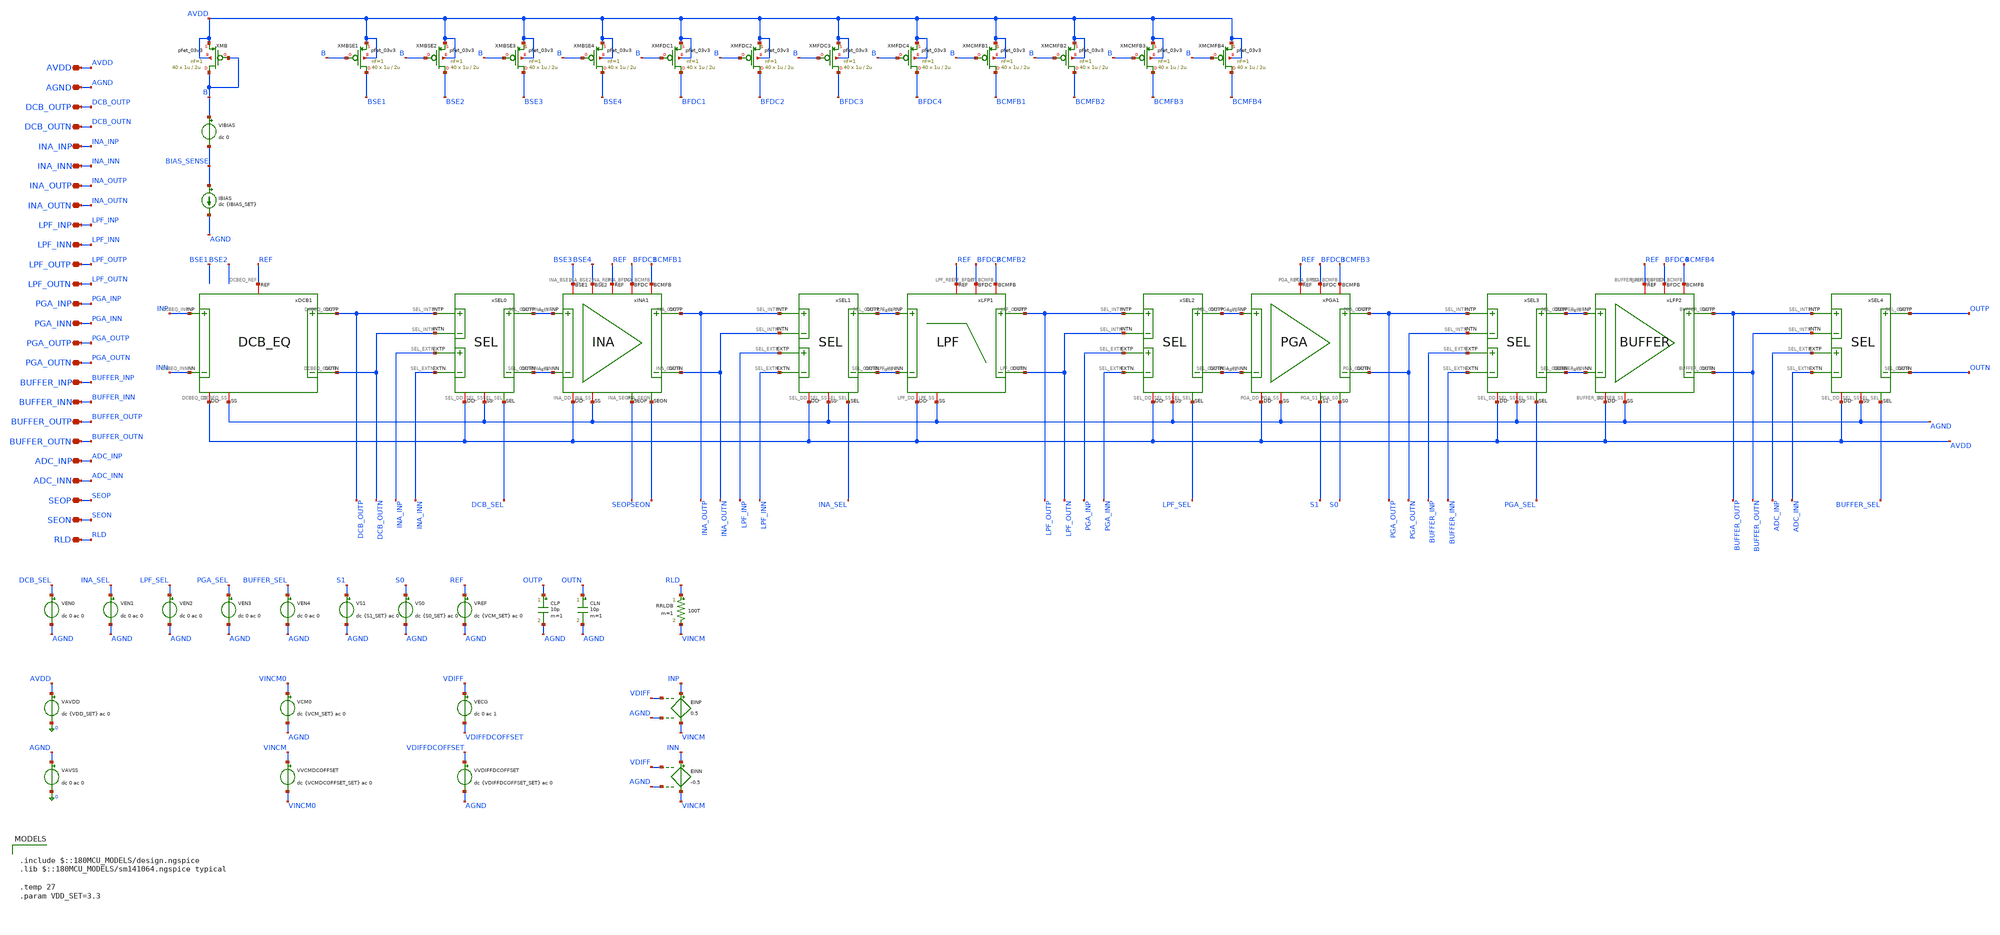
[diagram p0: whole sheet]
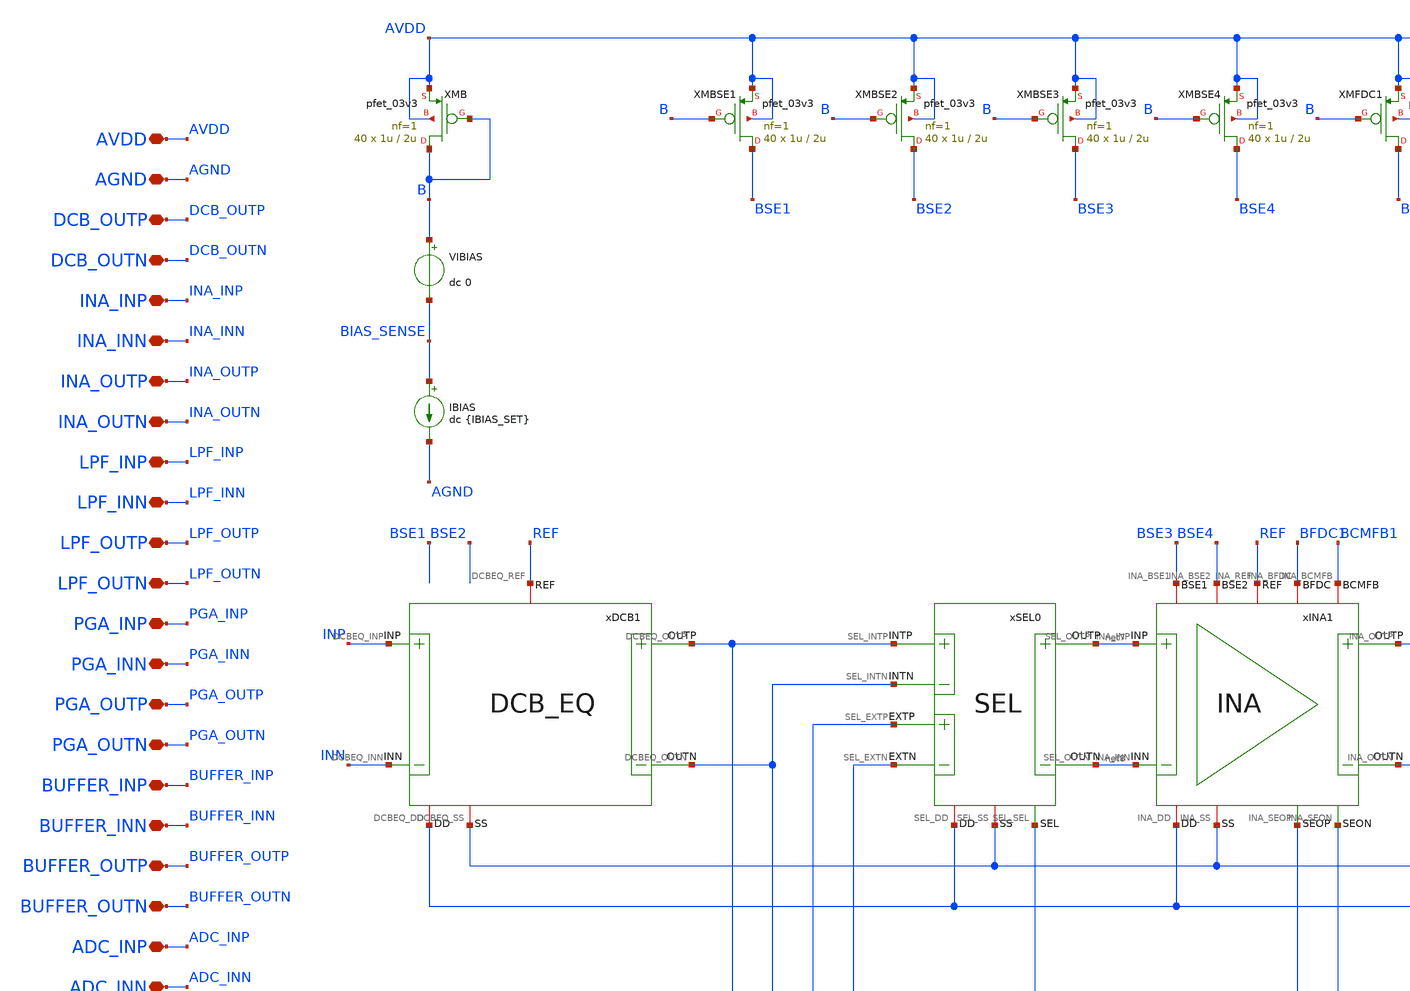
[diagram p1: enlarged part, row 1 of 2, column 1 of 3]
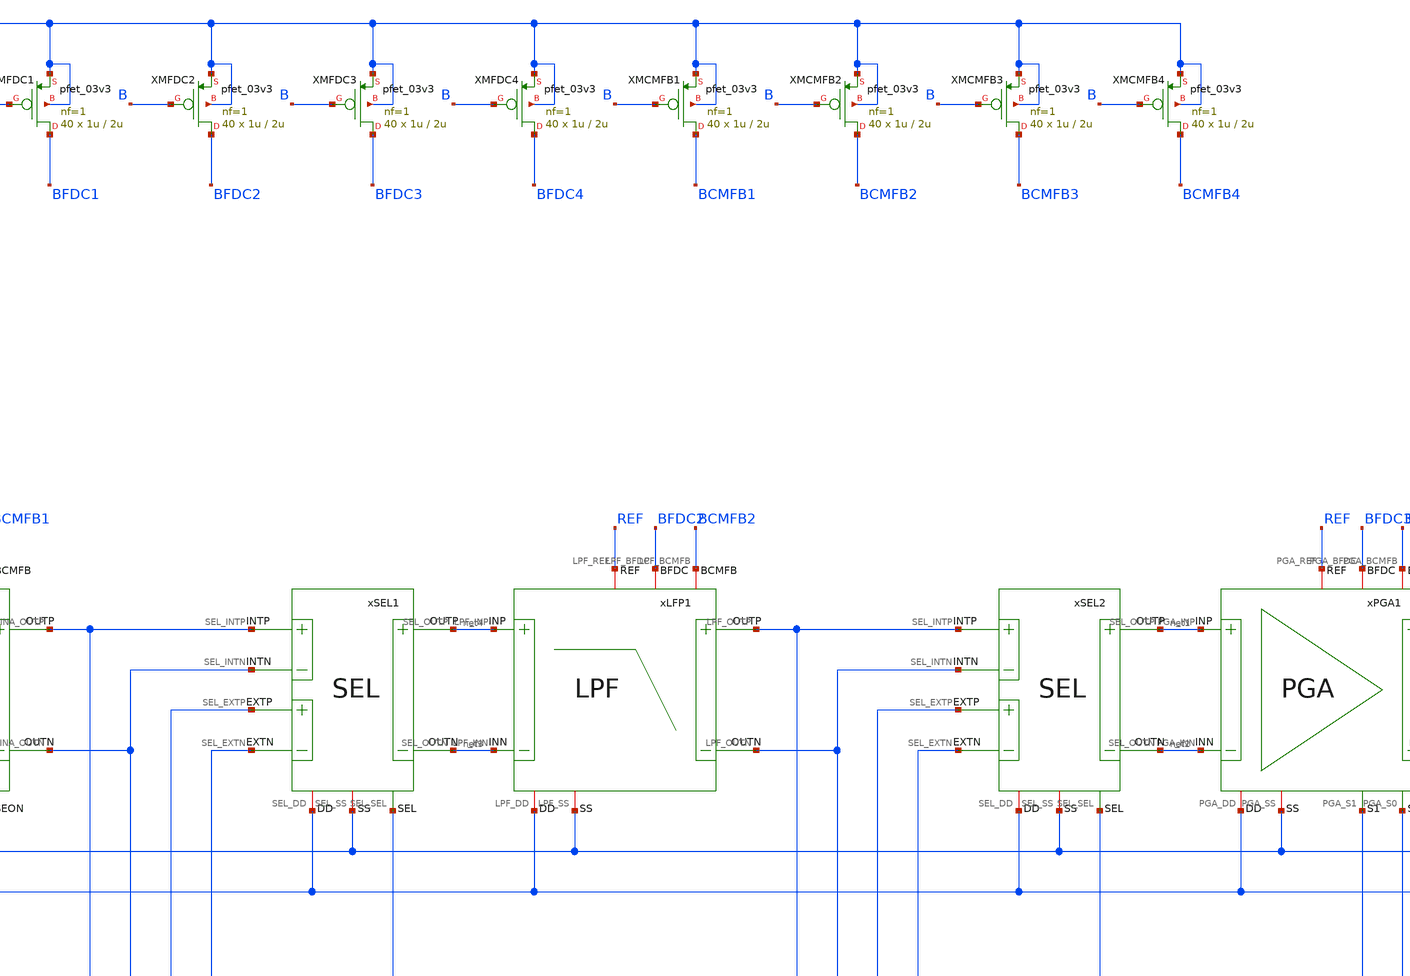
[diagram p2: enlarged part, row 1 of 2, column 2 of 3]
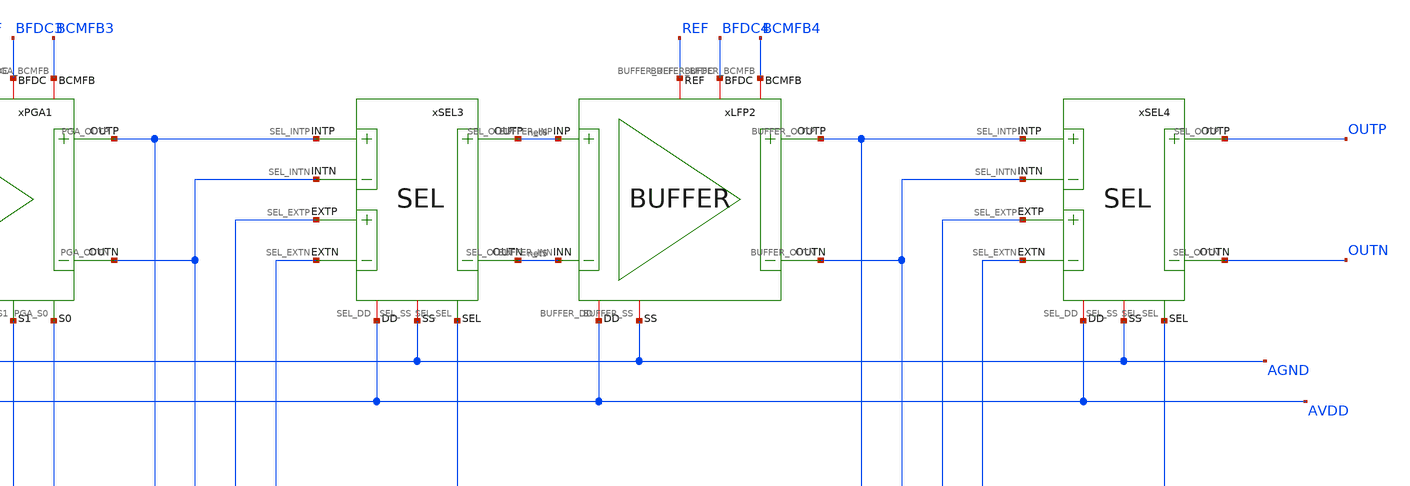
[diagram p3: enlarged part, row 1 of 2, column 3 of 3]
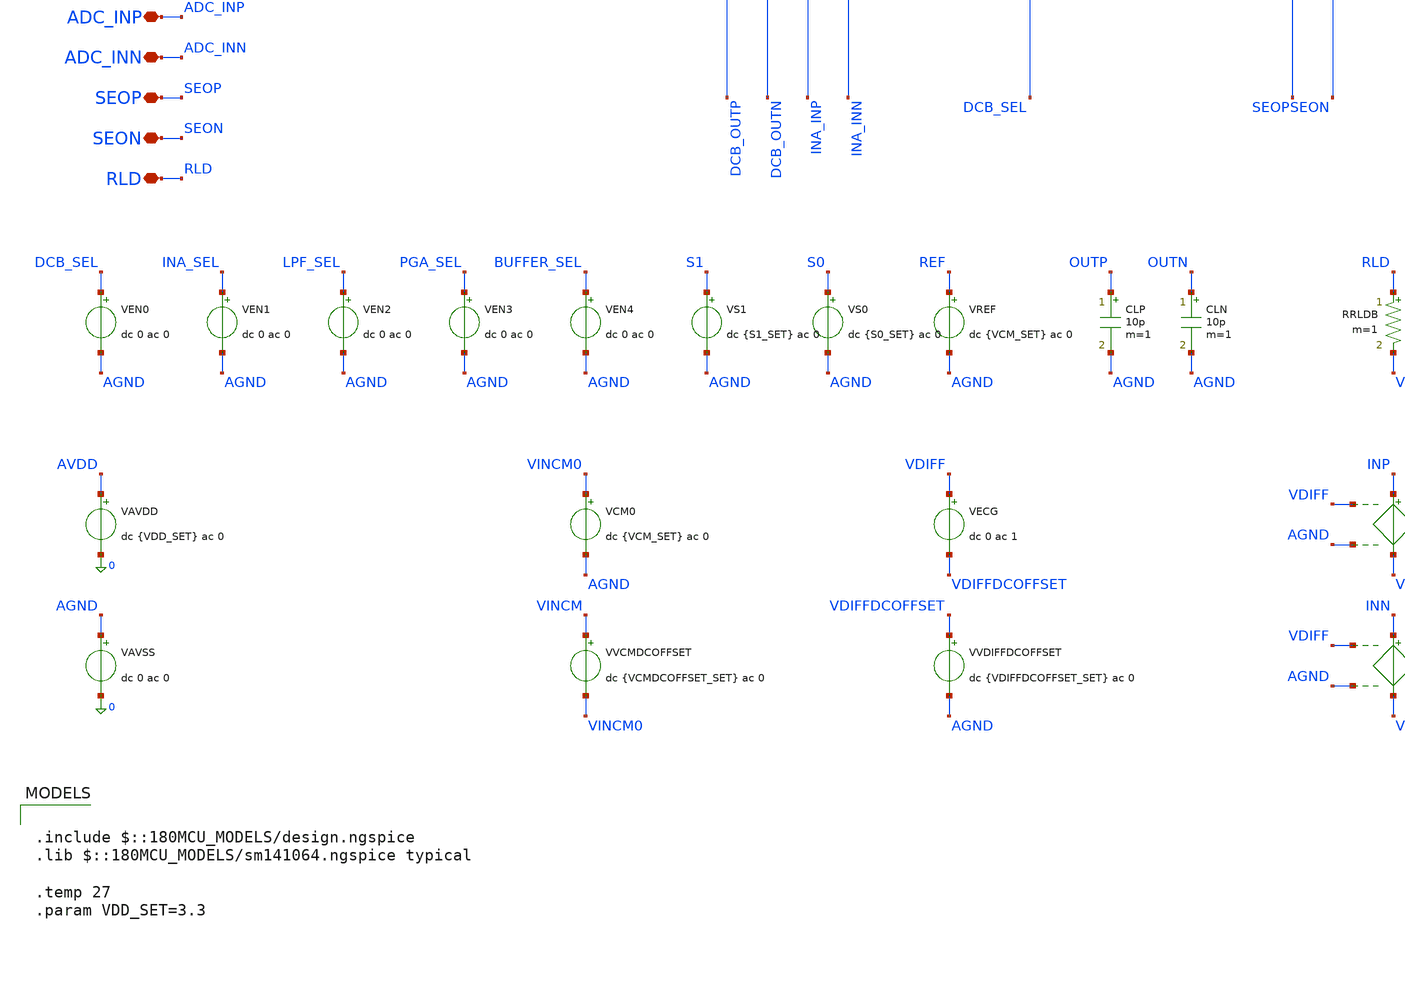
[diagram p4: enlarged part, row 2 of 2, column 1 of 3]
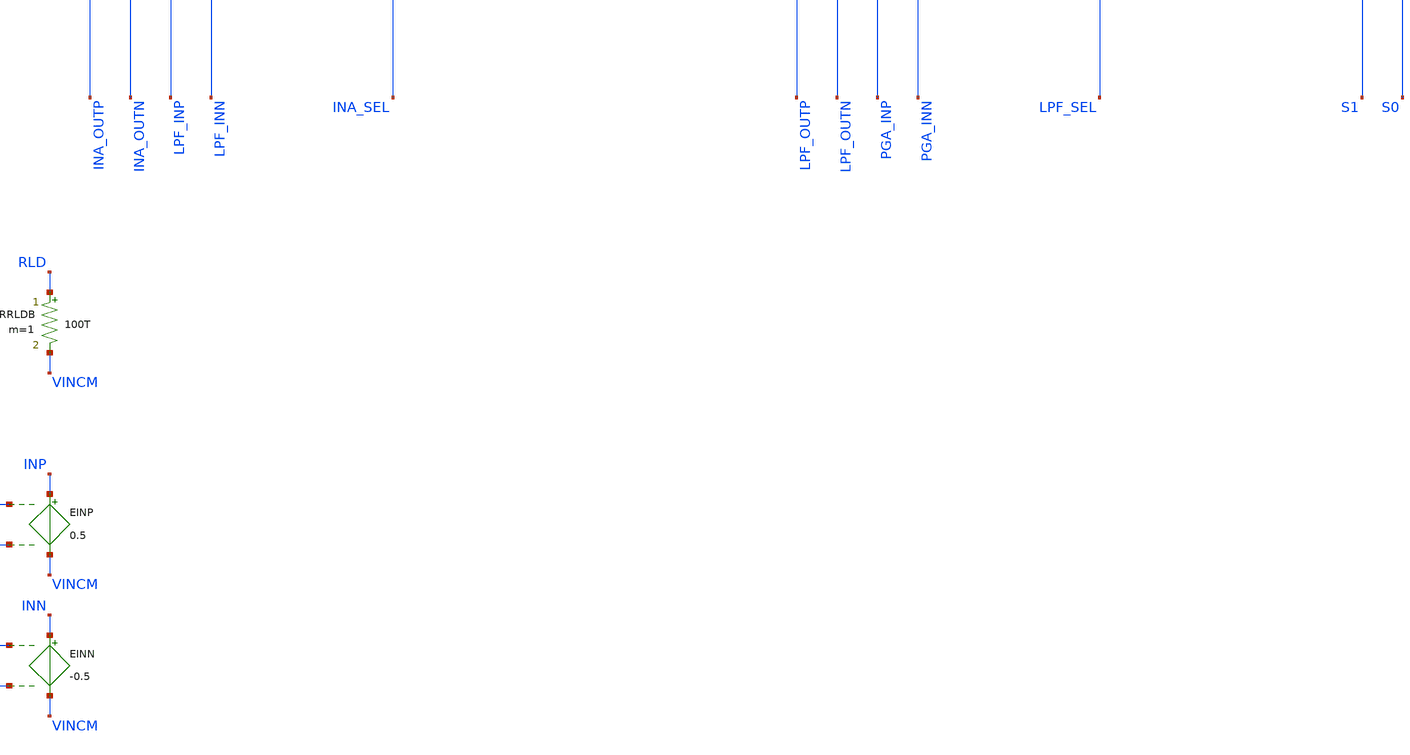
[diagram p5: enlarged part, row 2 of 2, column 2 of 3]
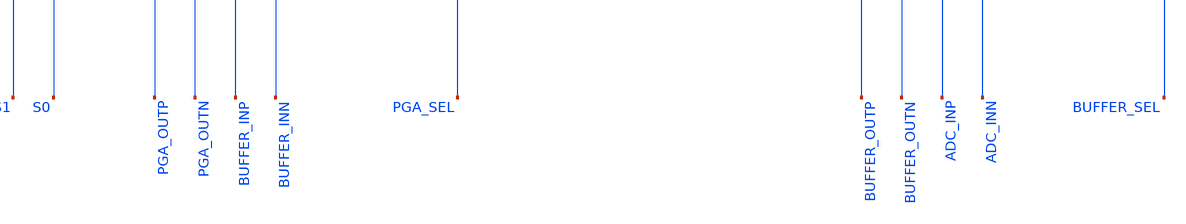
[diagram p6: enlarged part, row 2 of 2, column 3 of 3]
** sch_path: Design_Files/IC Design/Testbench/PATH/AC/PATH_TB_AC.sch
**.subckt PATH_TB_AC DCB_OUTP DCB_OUTN INA_INP INA_INN INA_OUTP INA_OUTN LPF_INP LPF_INN LPF_OUTP
*+ LPF_OUTN PGA_INP PGA_INN PGA_OUTP PGA_OUTN BUFFER_INP BUFFER_INN BUFFER_OUTP BUFFER_OUTN ADC_INP ADC_INN
*+ AVDD AGND SEOP SEON RLD
*.iopin DCB_OUTP
*.iopin DCB_OUTN
*.iopin INA_INP
*.iopin INA_INN
*.iopin INA_OUTP
*.iopin INA_OUTN
*.iopin LPF_INP
*.iopin LPF_INN
*.iopin LPF_OUTP
*.iopin LPF_OUTN
*.iopin PGA_INP
*.iopin PGA_INN
*.iopin PGA_OUTP
*.iopin PGA_OUTN
*.iopin BUFFER_INP
*.iopin BUFFER_INN
*.iopin BUFFER_OUTP
*.iopin BUFFER_OUTN
*.iopin ADC_INP
*.iopin ADC_INN
*.iopin AVDD
*.iopin AGND
*.iopin SEOP
*.iopin SEON
*.iopin RLD
CLP OUTP AGND 10p m=1
CLN OUTN AGND 10p m=1
VIBIAS B BIAS_SENSE dc 0
.save i(vibias)
IBIAS BIAS_SENSE AGND dc {IBIAS_SET}
VREF REF AGND dc {VCM_SET} ac 0
XMB B B AVDD AVDD pfet_03v3 L=2u W=1u nf=1 ad='int((nf+1)/2) * W/nf * 0.18u' as='int((nf+2)/2) * W/nf * 0.18u'
+ pd='2*int((nf+1)/2) * (W/nf + 0.18u)' ps='2*int((nf+2)/2) * (W/nf + 0.18u)' nrd='0.18u / W' nrs='0.18u / W'
+ sa=0 sb=0 sd=0 m=40
XMBSE3 BSE3 B AVDD AVDD pfet_03v3 L=2u W=1u nf=1 ad='int((nf+1)/2) * W/nf * 0.18u' as='int((nf+2)/2) * W/nf * 0.18u'
+ pd='2*int((nf+1)/2) * (W/nf + 0.18u)' ps='2*int((nf+2)/2) * (W/nf + 0.18u)' nrd='0.18u / W' nrs='0.18u / W'
+ sa=0 sb=0 sd=0 m=40
XMBSE4 BSE4 B AVDD AVDD pfet_03v3 L=2u W=1u nf=1 ad='int((nf+1)/2) * W/nf * 0.18u' as='int((nf+2)/2) * W/nf * 0.18u'
+ pd='2*int((nf+1)/2) * (W/nf + 0.18u)' ps='2*int((nf+2)/2) * (W/nf + 0.18u)' nrd='0.18u / W' nrs='0.18u / W'
+ sa=0 sb=0 sd=0 m=40
XMFDC1 BFDC1 B AVDD AVDD pfet_03v3 L=2u W=1u nf=1 ad='int((nf+1)/2) * W/nf * 0.18u' as='int((nf+2)/2) * W/nf * 0.18u'
+ pd='2*int((nf+1)/2) * (W/nf + 0.18u)' ps='2*int((nf+2)/2) * (W/nf + 0.18u)' nrd='0.18u / W' nrs='0.18u / W'
+ sa=0 sb=0 sd=0 m=40
XMFDC2 BFDC2 B AVDD AVDD pfet_03v3 L=2u W=1u nf=1 ad='int((nf+1)/2) * W/nf * 0.18u' as='int((nf+2)/2) * W/nf * 0.18u'
+ pd='2*int((nf+1)/2) * (W/nf + 0.18u)' ps='2*int((nf+2)/2) * (W/nf + 0.18u)' nrd='0.18u / W' nrs='0.18u / W'
+ sa=0 sb=0 sd=0 m=40
XMFDC3 BFDC3 B AVDD AVDD pfet_03v3 L=2u W=1u nf=1 ad='int((nf+1)/2) * W/nf * 0.18u' as='int((nf+2)/2) * W/nf * 0.18u'
+ pd='2*int((nf+1)/2) * (W/nf + 0.18u)' ps='2*int((nf+2)/2) * (W/nf + 0.18u)' nrd='0.18u / W' nrs='0.18u / W'
+ sa=0 sb=0 sd=0 m=40
XMFDC4 BFDC4 B AVDD AVDD pfet_03v3 L=2u W=1u nf=1 ad='int((nf+1)/2) * W/nf * 0.18u' as='int((nf+2)/2) * W/nf * 0.18u'
+ pd='2*int((nf+1)/2) * (W/nf + 0.18u)' ps='2*int((nf+2)/2) * (W/nf + 0.18u)' nrd='0.18u / W' nrs='0.18u / W'
+ sa=0 sb=0 sd=0 m=40
XMCMFB1 BCMFB1 B AVDD AVDD pfet_03v3 L=2u W=1u nf=1 ad='int((nf+1)/2) * W/nf * 0.18u' as='int((nf+2)/2) * W/nf * 0.18u'
+ pd='2*int((nf+1)/2) * (W/nf + 0.18u)' ps='2*int((nf+2)/2) * (W/nf + 0.18u)' nrd='0.18u / W' nrs='0.18u / W'
+ sa=0 sb=0 sd=0 m=40
XMCMFB2 BCMFB2 B AVDD AVDD pfet_03v3 L=2u W=1u nf=1 ad='int((nf+1)/2) * W/nf * 0.18u' as='int((nf+2)/2) * W/nf * 0.18u'
+ pd='2*int((nf+1)/2) * (W/nf + 0.18u)' ps='2*int((nf+2)/2) * (W/nf + 0.18u)' nrd='0.18u / W' nrs='0.18u / W'
+ sa=0 sb=0 sd=0 m=40
xLFP1 AVDD AGND net4 net3 LPF_OUTN BFDC2 LPF_OUTP BCMFB2 REF LPF
xPGA1 AVDD AGND net1 net2 PGA_OUTN BFDC3 PGA_OUTP BCMFB3 REF S1 S0 PGA
xSEL1 AVDD AGND INA_OUTP INA_OUTN net3 net4 LPF_INP LPF_INN INA_SEL SEL
xINA1 AVDD AGND net7 net8 INA_OUTN BFDC1 INA_OUTP BCMFB1 REF SEON SEOP BSE3 BSE4 INA
xSEL2 AVDD AGND LPF_OUTP LPF_OUTN net2 net1 PGA_INP PGA_INN LPF_SEL SEL
xSEL3 AVDD AGND PGA_OUTP PGA_OUTN net5 net6 BUFFER_INP BUFFER_INN PGA_SEL SEL
xSEL4 AVDD AGND BUFFER_OUTP BUFFER_OUTN OUTN OUTP ADC_INP ADC_INN BUFFER_SEL SEL
xLFP2 AVDD AGND net6 net5 BUFFER_OUTN BFDC4 BUFFER_OUTP BCMFB4 REF BUFFER
XMCMFB3 BCMFB3 B AVDD AVDD pfet_03v3 L=2u W=1u nf=1 ad='int((nf+1)/2) * W/nf * 0.18u' as='int((nf+2)/2) * W/nf * 0.18u'
+ pd='2*int((nf+1)/2) * (W/nf + 0.18u)' ps='2*int((nf+2)/2) * (W/nf + 0.18u)' nrd='0.18u / W' nrs='0.18u / W'
+ sa=0 sb=0 sd=0 m=40
XMCMFB4 BCMFB4 B AVDD AVDD pfet_03v3 L=2u W=1u nf=1 ad='int((nf+1)/2) * W/nf * 0.18u' as='int((nf+2)/2) * W/nf * 0.18u'
+ pd='2*int((nf+1)/2) * (W/nf + 0.18u)' ps='2*int((nf+2)/2) * (W/nf + 0.18u)' nrd='0.18u / W' nrs='0.18u / W'
+ sa=0 sb=0 sd=0 m=40
VEN1 INA_SEL AGND dc 0 ac 0
.save i(ven1)
VS0 S0 AGND dc {S0_SET} ac 0
VS1 S1 AGND dc {S1_SET} ac 0
xSEL0 AVDD AGND DCB_OUTP DCB_OUTN net8 net7 INA_INP INA_INN DCB_SEL SEL
VEN2 LPF_SEL AGND dc 0 ac 0
.save i(ven2)
VEN3 PGA_SEL AGND dc 0 ac 0
.save i(ven3)
VEN4 BUFFER_SEL AGND dc 0 ac 0
.save i(ven4)
VEN0 DCB_SEL AGND dc 0 ac 0
.save i(ven0)
xDCB1 AVDD AGND INP INN DCB_OUTP DCB_OUTN REF DCB_EQ
VAVDD AVDD 0 dc {VDD_SET} ac 0
.save i(vavdd)
VAVSS AGND 0 dc 0 ac 0
.save i(vavss)
VCM0 VINCM0 AGND dc {VCM_SET} ac 0
VVCMDCOFFSET VINCM VINCM0 dc {VCMDCOFFSET_SET} ac 0
VECG VDIFF VDIFFDCOFFSET dc 0 ac 1
VVDIFFDCOFFSET VDIFFDCOFFSET AGND dc {VDIFFDCOFFSET_SET} ac 0
EINP INP VINCM VDIFF AGND 0.5
EINN INN VINCM VDIFF AGND -0.5
RRLDB RLD VINCM 100T m=1
XMBSE1 BSE1 B AVDD AVDD pfet_03v3 L=2u W=1u nf=1 ad='int((nf+1)/2) * W/nf * 0.18u' as='int((nf+2)/2) * W/nf * 0.18u'
+ pd='2*int((nf+1)/2) * (W/nf + 0.18u)' ps='2*int((nf+2)/2) * (W/nf + 0.18u)' nrd='0.18u / W' nrs='0.18u / W'
+ sa=0 sb=0 sd=0 m=40
XMBSE2 BSE2 B AVDD AVDD pfet_03v3 L=2u W=1u nf=1 ad='int((nf+1)/2) * W/nf * 0.18u' as='int((nf+2)/2) * W/nf * 0.18u'
+ pd='2*int((nf+1)/2) * (W/nf + 0.18u)' ps='2*int((nf+2)/2) * (W/nf + 0.18u)' nrd='0.18u / W' nrs='0.18u / W'
+ sa=0 sb=0 sd=0 m=40
**** begin user architecture code

.include $::180MCU_MODELS/design.ngspice
.lib $::180MCU_MODELS/sm141064.ngspice typical

.temp 27
.param VDD_SET=3.3



.param VCM_SET={VDD_SET/2}

.param VCMDCOFFSET_SET=0
.param VDIFFDCOFFSET_SET=0

.param IBIAS_SET=40u

.param S1_SET=3.3
.param S0_SET=3.3

.options method=gear
.options sparse

.options gmin=1e-12
.options rshunt=100T

.options reltol=1e-3
.options abstol=1e-12
.options vntol=1u
.options chgtol=1e-14

.options itl1=2000
.options itl2=1000
.options itl4=2000

.nodeset v(B)=2.3

.nodeset v(INP)={VCM_SET}
.nodeset v(INN)={VCM_SET}

.nodeset v(DCB_OUTP)={VCM_SET}
.nodeset v(DCB_OUTN)={VCM_SET}

.nodeset v(INA_OUTP)={VCM_SET}
.nodeset v(INA_OUTN)={VCM_SET}

.nodeset v(LPF_OUTP)={VCM_SET}
.nodeset v(LPF_OUTN)={VCM_SET}

.nodeset v(PGA_OUTP)={VCM_SET}
.nodeset v(PGA_OUTN)={VCM_SET}

.nodeset v(BUFFER_OUTP)={VCM_SET}
.nodeset v(BUFFER_OUTN)={VCM_SET}

.nodeset v(OUTP)={VCM_SET}
.nodeset v(OUTN)={VCM_SET}

.nodeset v(RLD)={VCM_SET}

.save all





.control

destroy all

set noaskquit
set wr_singlescale
unset wr_vecnames
set appendwrite
set units=degrees

option numdgt=15
option sparse

shell mkdir -p
+ /foss/designs/ECG_Acquisition_IC/Measurement_Results/IC_Simulation/PATH/NOM.Result_txt

shell rm -f
+ /foss/designs/ECG_Acquisition_IC/Measurement_Results/IC_Simulation/PATH/NOM.Result_txt/NOM.op.txt
shell rm -f
+ /foss/designs/ECG_Acquisition_IC/Measurement_Results/IC_Simulation/PATH/NOM.Result_txt/NOM.diff_ac.txt
shell rm -f
+ /foss/designs/ECG_Acquisition_IC/Measurement_Results/IC_Simulation/PATH/NOM.Result_txt/NOM.cmrr_ac.txt
shell rm -f
+ /foss/designs/ECG_Acquisition_IC/Measurement_Results/IC_Simulation/PATH/NOM.Result_txt/NOM.psrrp_ac.txt
shell rm -f
+ /foss/designs/ECG_Acquisition_IC/Measurement_Results/IC_Simulation/PATH/NOM.Result_txt/NOM.psrrn_ac.txt


* OP: G2 and G16
foreach gaincfg 0 1

    if $gaincfg = 0
        alterparam S1_SET=0
        alterparam S0_SET=0
    else
        alterparam S1_SET=3.3
        alterparam S0_SET=3.3
    end

    reset
    save all

    alter @VECG[ACMAG]=0
    alter @VECG[ACPHASE]=0

    alter @VCM0[ACMAG]=0
    alter @VCM0[ACPHASE]=0

    alter @VAVDD[ACMAG]=0
    alter @VAVDD[ACPHASE]=0

    alter @VAVSS[ACMAG]=0
    alter @VAVSS[ACPHASE]=0

    op

    let op_index=0

    if $gaincfg = 0
        let op_pga_gain=op_index*0+2
    else
        let op_pga_gain=op_index*0+16
    end

    let op_vdd=v(AVDD)-v(AGND)

    let op_vinp=v(INP)-v(AGND)
    let op_vinn=v(INN)-v(AGND)

    let op_vin_cm=0.5*(v(INP)+v(INN))-v(AGND)
    let op_vin_diff=v(INP)-v(INN)

    let op_outp=v(OUTP)-v(AGND)
    let op_outn=v(OUTN)-v(AGND)

    let op_vout_cm=0.5*(v(OUTP)+v(OUTN))-v(AGND)
    let op_vout_diff=v(OUTP)-v(OUTN)

    let op_rld=v(RLD)-v(AGND)
    let op_ref=v(REF)-v(AGND)

    let op_ibias=abs(vibias#branch)
    let op_idd=abs(vavdd#branch)
    let op_power=op_vdd*op_idd

    setscale op_index

    wrdata
+ /foss/designs/ECG_Acquisition_IC/Measurement_Results/IC_Simulation/PATH/NOM.Result_txt/NOM.op.txt op_pga_gain op_vdd op_vinp op_vinn op_vin_cm op_vin_diff op_outp op_outn op_vout_cm op_vout_diff
+ op_rld op_ref op_ibias op_idd op_power

    destroy $curplot

end


* Differential AC: G2 and G16
foreach gaincfg 0 1

    if $gaincfg = 0
        alterparam S1_SET=0
        alterparam S0_SET=0
    else
        alterparam S1_SET=3.3
        alterparam S0_SET=3.3
    end

    reset
    save all

    alter @VECG[ACMAG]=1
    alter @VECG[ACPHASE]=0

    alter @VCM0[ACMAG]=0
    alter @VCM0[ACPHASE]=0

    alter @VAVDD[ACMAG]=0
    alter @VAVDD[ACPHASE]=0

    alter @VAVSS[ACMAG]=0
    alter @VAVSS[ACPHASE]=0

    ac dec 200 0.001 10k

    if $gaincfg = 0
        let ac_pga_gain=frequency*0+2
    else
        let ac_pga_gain=frequency*0+16
    end

    let ac_vin_diff=v(INP)-v(INN)
    let ac_vout_diff=v(OUTP)-v(OUTN)
    let ac_vout_cm=0.5*(v(OUTP)+v(OUTN))-v(AGND)

    let ac_hdiff=ac_vout_diff/ac_vin_diff

    let vin_diff_real=real(ac_vin_diff)
    let vin_diff_imag=imag(ac_vin_diff)
    let vin_diff_mag=mag(ac_vin_diff)
    let vin_diff_phase=ph(ac_vin_diff)

    let vout_diff_real=real(ac_vout_diff)
    let vout_diff_imag=imag(ac_vout_diff)
    let vout_diff_mag=mag(ac_vout_diff)
    let vout_diff_phase=ph(ac_vout_diff)

    let vout_cm_real=real(ac_vout_cm)
    let vout_cm_imag=imag(ac_vout_cm)

    let hdiff_real=real(ac_hdiff)
    let hdiff_imag=imag(ac_hdiff)
    let hdiff_mag=mag(ac_hdiff)
    let hdiff_db=db(ac_hdiff)
    let hdiff_phase=ph(ac_hdiff)

    setscale frequency

    wrdata
+ /foss/designs/ECG_Acquisition_IC/Measurement_Results/IC_Simulation/PATH/NOM.Result_txt/NOM.diff_ac.txt ac_pga_gain vin_diff_real vin_diff_imag vin_diff_mag vin_diff_phase vout_diff_real vout_diff_imag
+ vout_diff_mag vout_diff_phase vout_cm_real vout_cm_imag hdiff_real hdiff_imag hdiff_mag hdiff_db hdiff_phase

    destroy $curplot

end


* CMRR AC: G2 and G16
foreach gaincfg 0 1

    if $gaincfg = 0
        alterparam S1_SET=0
        alterparam S0_SET=0
    else
        alterparam S1_SET=3.3
        alterparam S0_SET=3.3
    end

    reset
    save all

    alter @VECG[ACMAG]=0
    alter @VECG[ACPHASE]=0

    alter @VCM0[ACMAG]=1
    alter @VCM0[ACPHASE]=0

    alter @VAVDD[ACMAG]=0
    alter @VAVDD[ACPHASE]=0

    alter @VAVSS[ACMAG]=0
    alter @VAVSS[ACPHASE]=0

    ac dec 200 0.001 10k

    if $gaincfg = 0
        let ac_pga_gain=frequency*0+2
    else
        let ac_pga_gain=frequency*0+16
    end

    let ac_vin_cm=0.5*(v(INP)+v(INN))-v(AGND)
    let ac_vout_diff=v(OUTP)-v(OUTN)
    let ac_vout_cm=0.5*(v(OUTP)+v(OUTN))-v(AGND)

    let ac_hcm_diff=ac_vout_diff/ac_vin_cm

    let vin_cm_real=real(ac_vin_cm)
    let vin_cm_imag=imag(ac_vin_cm)
    let vin_cm_mag=mag(ac_vin_cm)
    let vin_cm_phase=ph(ac_vin_cm)

    let vout_diff_real=real(ac_vout_diff)
    let vout_diff_imag=imag(ac_vout_diff)

    let vout_cm_real=real(ac_vout_cm)
    let vout_cm_imag=imag(ac_vout_cm)

    let hcm_diff_real=real(ac_hcm_diff)
    let hcm_diff_imag=imag(ac_hcm_diff)
    let hcm_diff_mag=mag(ac_hcm_diff)
    let hcm_diff_db=db(ac_hcm_diff)
    let hcm_diff_phase=ph(ac_hcm_diff)

    setscale frequency

    wrdata
+ /foss/designs/ECG_Acquisition_IC/Measurement_Results/IC_Simulation/PATH/NOM.Result_txt/NOM.cmrr_ac.txt ac_pga_gain vin_cm_real vin_cm_imag vin_cm_mag vin_cm_phase vout_diff_real vout_diff_imag
+ vout_cm_real vout_cm_imag hcm_diff_real hcm_diff_imag hcm_diff_mag hcm_diff_db hcm_diff_phase

    destroy $curplot

end


* PSRR+ AC: G2 and G16
foreach gaincfg 0 1

    if $gaincfg = 0
        alterparam S1_SET=0
        alterparam S0_SET=0
    else
        alterparam S1_SET=3.3
        alterparam S0_SET=3.3
    end

    reset
    save all

    alter @VECG[ACMAG]=0
    alter @VECG[ACPHASE]=0

    alter @VCM0[ACMAG]=0
    alter @VCM0[ACPHASE]=0

    alter @VAVDD[ACMAG]=1
    alter @VAVDD[ACPHASE]=0

    alter @VAVSS[ACMAG]=0
    alter @VAVSS[ACPHASE]=0

    ac dec 200 0.001 10k

    if $gaincfg = 0
        let ac_pga_gain=frequency*0+2
    else
        let ac_pga_gain=frequency*0+16
    end

    let ac_supply=v(AVDD)-v(AGND)
    let ac_vout_diff=v(OUTP)-v(OUTN)
    let ac_vout_cm=0.5*(v(OUTP)+v(OUTN))-v(AGND)

    let ac_hpsrrp=ac_vout_diff/ac_supply

    let supply_real=real(ac_supply)
    let supply_imag=imag(ac_supply)
    let supply_mag=mag(ac_supply)
    let supply_phase=ph(ac_supply)

    let vout_diff_real=real(ac_vout_diff)
    let vout_diff_imag=imag(ac_vout_diff)

    let vout_cm_real=real(ac_vout_cm)
    let vout_cm_imag=imag(ac_vout_cm)

    let hpsrrp_real=real(ac_hpsrrp)
    let hpsrrp_imag=imag(ac_hpsrrp)
    let hpsrrp_mag=mag(ac_hpsrrp)
    let hpsrrp_db=db(ac_hpsrrp)
    let hpsrrp_phase=ph(ac_hpsrrp)

    setscale frequency

    wrdata
+ /foss/designs/ECG_Acquisition_IC/Measurement_Results/IC_Simulation/PATH/NOM.Result_txt/NOM.psrrp_ac.txt ac_pga_gain supply_real supply_imag supply_mag supply_phase vout_diff_real vout_diff_imag
+ vout_cm_real vout_cm_imag hpsrrp_real hpsrrp_imag hpsrrp_mag hpsrrp_db hpsrrp_phase

    destroy $curplot

end


* PSRR- AC: G2 and G16
foreach gaincfg 0 1

    if $gaincfg = 0
        alterparam S1_SET=0
        alterparam S0_SET=0
    else
        alterparam S1_SET=3.3
        alterparam S0_SET=3.3
    end

    reset
    save all

    alter @VECG[ACMAG]=0
    alter @VECG[ACPHASE]=0

    alter @VCM0[ACMAG]=0
    alter @VCM0[ACPHASE]=0

    alter @VAVDD[ACMAG]=0
    alter @VAVDD[ACPHASE]=0

    alter @VAVSS[ACMAG]=1
    alter @VAVSS[ACPHASE]=0

    ac dec 200 0.001 10k

    if $gaincfg = 0
        let ac_pga_gain=frequency*0+2
    else
        let ac_pga_gain=frequency*0+16
    end

    let ac_supply=v(AGND)
    let ac_vout_diff=v(OUTP)-v(OUTN)
    let ac_vout_cm=0.5*(v(OUTP)+v(OUTN))-v(AGND)

    let ac_hpsrrn=ac_vout_diff/ac_supply

    let supply_real=real(ac_supply)
    let supply_imag=imag(ac_supply)
    let supply_mag=mag(ac_supply)
    let supply_phase=ph(ac_supply)

    let vout_diff_real=real(ac_vout_diff)
    let vout_diff_imag=imag(ac_vout_diff)

    let vout_cm_real=real(ac_vout_cm)
    let vout_cm_imag=imag(ac_vout_cm)

    let hpsrrn_real=real(ac_hpsrrn)
    let hpsrrn_imag=imag(ac_hpsrrn)
    let hpsrrn_mag=mag(ac_hpsrrn)
    let hpsrrn_db=db(ac_hpsrrn)
    let hpsrrn_phase=ph(ac_hpsrrn)

    setscale frequency

    wrdata
+ /foss/designs/ECG_Acquisition_IC/Measurement_Results/IC_Simulation/PATH/NOM.Result_txt/NOM.psrrn_ac.txt ac_pga_gain supply_real supply_imag supply_mag supply_phase vout_diff_real vout_diff_imag
+ vout_cm_real vout_cm_imag hpsrrn_real hpsrrn_imag hpsrrn_mag hpsrrn_db hpsrrn_phase

    destroy $curplot

end


* Last simulated gain is already G16

quit
.endc


**** end user architecture code
**.ends

* expanding   symbol:  ECG_Acquisition_IC/Design_Files/IC Design/Schematic/LPF/LPF.sym # of pins=9
** sym_path: Design_Files/IC Design/Schematic/LPF/LPF.sym
** sch_path: Design_Files/IC Design/Schematic/LPF/LPF.sch
.subckt LPF LPF_DD LPF_SS LPF_INP LPF_INN LPF_OUTN LPF_BFDC LPF_OUTP LPF_BCMFB LPF_REF
*.iopin LPF_DD
*.iopin LPF_SS
*.ipin LPF_INP
*.ipin LPF_INN
*.opin LPF_OUTP
*.iopin LPF_BFDC
*.opin LPF_OUTN
*.iopin LPF_BCMFB
*.iopin LPF_REF
RFBP net1 LPF_OUTN 3.7Meg m=1
xFDOTA1 LPF_DD LPF_SS net1 net2 LPF_OUTN LPF_BFDC LPF_OUTP LPF_BCMFB LPF_REF LPF_VOCM FD_OTA
RINN LPF_INN net2 3.7Meg m=1
RINP LPF_INP net1 3.7Meg m=1
RFBN net2 LPF_OUTP 3.7Meg m=1
CLPFP net1 LPF_OUTN 20p m=5
CLPFN net2 LPF_OUTP 20p m=5
.ends


* expanding   symbol:  ECG_Acquisition_IC/Design_Files/IC Design/Schematic/PGA/PGA.sym # of pins=11
** sym_path: Design_Files/IC Design/Schematic/PGA/PGA.sym
** sch_path: Design_Files/IC Design/Schematic/PGA/PGA.sch
.subckt PGA PGA_DD PGA_SS PGA_INP PGA_INN PGA_OUTN PGA_BFDC PGA_OUTP PGA_BCMFB PGA_REF PGA_S1 PGA_S0
*.iopin PGA_DD
*.iopin PGA_SS
*.ipin PGA_INP
*.ipin PGA_INN
*.opin PGA_OUTP
*.iopin PGA_BFDC
*.opin PGA_OUTN
*.iopin PGA_BCMFB
*.iopin PGA_REF
*.ipin PGA_S0
*.ipin PGA_S1
RFBP1 net2 net1 40k m=1
xFDOTA1 PGA_DD PGA_SS net2 net8 PGA_OUTN PGA_BFDC PGA_OUTP PGA_BCMFB PGA_REF PGA_VOCM FD_OTA
RFBP2 net1 net3 40k m=1
RFBP3 net3 net4 120k m=1
RFBP4 net4 PGA_OUTN 120k m=1
RINN PGA_INN net8 20k m=1
RINP PGA_INP net2 20k m=1
xTG1 PGA_DD PGA_SS net1 net3 S0B PGA_S0 TG
xTG3 PGA_DD PGA_SS net3 PGA_OUTN S1B PGA_S1 TG
xINV1 PGA_DD PGA_SS PGA_S0 S0B INV
xTG2 PGA_DD PGA_SS net3 net4 S0B PGA_S0 TG
RFBN1 net8 net5 40k m=1
RFBN2 net5 net6 40k m=1
RFBN3 net6 net7 120k m=1
RFBN4 net7 PGA_OUTP 120k m=1
xTG4 PGA_DD PGA_SS net5 net6 S0B PGA_S0 TG
xTG5 PGA_DD PGA_SS net6 net7 S0B PGA_S0 TG
xINV2 PGA_DD PGA_SS PGA_S1 S1B INV
xTG6 PGA_DD PGA_SS net6 PGA_OUTP S1B PGA_S1 TG
.ends


* expanding   symbol:  ECG_Acquisition_IC/Design_Files/IC Design/Schematic/SEL/SEL.sym # of pins=9
** sym_path: Design_Files/IC Design/Schematic/SEL/SEL.sym
** sch_path: Design_Files/IC Design/Schematic/SEL/SEL.sch
.subckt SEL SEL_DD SEL_SS SEL_INTP SEL_INTN SEL_OUTN SEL_OUTP SEL_EXTP SEL_EXTN SEL_SEL
*.iopin SEL_DD
*.iopin SEL_SS
*.ipin SEL_INTP
*.ipin SEL_INTN
*.iopin SEL_OUTP
*.iopin SEL_OUTN
*.ipin SEL_EXTP
*.ipin SEL_EXTN
*.ipin SEL_SEL
xINV1 SEL_DD SEL_SS SEL_SEL SELB INV
xTG1 SEL_DD SEL_SS SEL_EXTP SEL_OUTP SEL_SEL SELB TG
xTG2 SEL_DD SEL_SS SEL_INTP SEL_OUTP SELB SEL_SEL TG
xTG3 SEL_DD SEL_SS SEL_EXTN SEL_OUTN SEL_SEL SELB TG
xTG4 SEL_DD SEL_SS SEL_INTN SEL_OUTN SELB SEL_SEL TG
.ends


* expanding   symbol:  ECG_Acquisition_IC/Design_Files/IC Design/Schematic/INA/INA.sym # of pins=13
** sym_path: Design_Files/IC Design/Schematic/INA/INA.sym
** sch_path: Design_Files/IC Design/Schematic/INA/INA.sch
.subckt INA INA_DD INA_SS INA_INP INA_INN INA_OUTN INA_BFDC INA_OUTP INA_BCMFB INA_REF INA_SEON
+ INA_SEOP INA_BSE1 INA_BSE2
*.iopin INA_DD
*.iopin INA_SS
*.ipin INA_INP
*.ipin INA_INN
*.opin INA_OUTP
*.iopin INA_BFDC
*.opin INA_OUTN
*.iopin INA_BCMFB
*.iopin INA_REF
*.iopin INA_BSE1
*.iopin INA_SEON
*.iopin INA_SEOP
*.iopin INA_BSE2
RFDFBP INA_FDINP INA_OUTN 40k m=1
xFDOTA1 INA_DD INA_SS INA_FDINP INA_FDINN INA_OUTN INA_BFDC INA_OUTP INA_BCMFB INA_REF INA_VOCM
+ FD_OTA
xSEOTA1 INA_DD INA_SS INA_INP INA_SEFP INA_SEOP INA_BSE1 SE_OTA
xSEOTA2 INA_DD INA_SS INA_INN INA_SEFN INA_SEON INA_BSE2 SE_OTA
RFDFBN INA_FDINN INA_OUTP 40k m=1
RFDINP INA_SEOP INA_FDINP 10k m=1
RFDINN INA_SEON INA_FDINN 10k m=1
RSEFP INA_SEOP INA_SEFP 118k m=1
RSEFN INA_SEON INA_SEFN 118k m=1
RSEG INA_SEFP INA_SEFN 4k m=1
.ends


* expanding   symbol:  ECG_Acquisition_IC/Design_Files/IC Design/Schematic/BUFFER/BUFFER.sym # of
*+ pins=9
** sym_path: Design_Files/IC Design/Schematic/BUFFER/BUFFER.sym
** sch_path: Design_Files/IC Design/Schematic/BUFFER/BUFFER.sch
.subckt BUFFER BUFFER_DD BUFFER_SS BUFFER_INP BUFFER_INN BUFFER_OUTN BUFFER_BFDC BUFFER_OUTP
+ BUFFER_BCMFB BUFFER_REF
*.iopin BUFFER_DD
*.iopin BUFFER_SS
*.ipin BUFFER_INP
*.ipin BUFFER_INN
*.opin BUFFER_OUTP
*.iopin BUFFER_BFDC
*.opin BUFFER_OUTN
*.iopin BUFFER_BCMFB
*.iopin BUFFER_REF
RFBP net1 BUFFER_OUTN 20k m=1
xFDOTA1 BUFFER_DD BUFFER_SS net1 net2 BUFFER_OUTN BUFFER_BFDC BUFFER_OUTP BUFFER_BCMFB BUFFER_REF
+ BUFFER_VOCM FD_OTA
RINN BUFFER_INN net2 20k m=1
RINP BUFFER_INP net1 20k m=1
RFBN net2 BUFFER_OUTP 20k m=1
.ends


* expanding   symbol:  ECG_Acquisition_IC/Design_Files/IC Design/Schematic/DCB_EQ/DCB_EQ.sym # of
*+ pins=7
** sym_path: Design_Files/IC Design/Schematic/DCB_EQ/DCB_EQ.sym
** sch_path: Design_Files/IC Design/Schematic/DCB_EQ/DCB_EQ.sch
.subckt DCB_EQ DCBEQ_DD DCBEQ_SS DCBEQ_INP DCBEQ_INN DCBEQ_OUTP DCBEQ_OUTN DCBEQ_REF
*.iopin DCBEQ_DD
*.iopin DCBEQ_SS
*.ipin DCBEQ_INP
*.ipin DCBEQ_INN
*.opin DCBEQ_OUTP
*.opin DCBEQ_OUTN
*.iopin DCBEQ_REF
CBP DCBEQ_INP DCBEQ_OUTP 20p m=25
CBN DCBEQ_INN DCBEQ_OUTN 20p m=25
REQP DCBEQ_OUTP DCBEQ_REF 20G m=1
REQN DCBEQ_OUTN DCBEQ_REF 20G m=1
.ends


* expanding   symbol:  ECG_Acquisition_IC/Design_Files/IC Design/Schematic/FD_OTA/FDOTA/FD_OTA.sym #
*+ of pins=10
** sym_path: Design_Files/IC Design/Schematic/FD_OTA/FDOTA/FD_OTA.sym
** sch_path: Design_Files/IC Design/Schematic/FD_OTA/FDOTA/FD_OTA.sch
.subckt FD_OTA FDOTA_DD FDOTA_SS FDOTA_INP FDOTA_INN FDOTA_OUTN FDOTA_BFDC FDOTA_OUTP FDOTA_BCMFB
+ FDOTA_REF FDOTA_VOCM
*.iopin FDOTA_DD
*.iopin FDOTA_SS
*.ipin FDOTA_INP
*.ipin FDOTA_INN
*.opin FDOTA_OUTP
*.iopin FDOTA_BFDC
*.opin FDOTA_OUTN
*.iopin FDOTA_BCMFB
*.iopin FDOTA_REF
*.iopin FDOTA_VOCM
R1 FDOTA_OUTP FDOTA_VOCM 100k m=1
R2 FDOTA_VOCM FDOTA_OUTN 100k m=1
C1 FDOTA_OUTP FDOTA_VOCM 50f m=1
C2 FDOTA_VOCM FDOTA_OUTN 50f m=1
xFDC1 FDOTA_DD FDOTA_SS FDOTA_INP FDOTA_INN FDOTA_OUTN FDOTA_BFDC FDOTA_OUTP FDOTA_VCMFB FDC
xCMFB1 FDOTA_DD FDOTA_SS FDOTA_VOCM FDOTA_REF FDOTA_VCMFB FDOTA_BCMFB CMFB
.ends


* expanding   symbol:  ECG_Acquisition_IC/Design_Files/IC Design/Schematic/TG/TG.sym # of pins=6
** sym_path: Design_Files/IC Design/Schematic/TG/TG.sym
** sch_path: Design_Files/IC Design/Schematic/TG/TG.sch
.subckt TG TG_DD TG_SS TG_A TG_B TG_SEL TG_SELB
*.iopin TG_DD
*.iopin TG_SS
*.iopin TG_A
*.iopin TG_B
*.ipin TG_SEL
*.ipin TG_SELB
XMTGP TG_B TG_SELB TG_A TG_DD pfet_03v3 L=0.5u W=10u nf=1 ad='int((nf+1)/2) * W/nf * 0.18u' as='int((nf+2)/2) * W/nf * 0.18u'
+ pd='2*int((nf+1)/2) * (W/nf + 0.18u)' ps='2*int((nf+2)/2) * (W/nf + 0.18u)' nrd='0.18u / W' nrs='0.18u / W'
+ sa=0 sb=0 sd=0 m=1
XMTGN TG_A TG_SEL TG_B TG_SS nfet_03v3 L=0.5u W=5u nf=1 ad='int((nf+1)/2) * W/nf * 0.18u' as='int((nf+2)/2) * W/nf * 0.18u'
+ pd='2*int((nf+1)/2) * (W/nf + 0.18u)' ps='2*int((nf+2)/2) * (W/nf + 0.18u)' nrd='0.18u / W' nrs='0.18u / W'
+ sa=0 sb=0 sd=0 m=1
.ends


* expanding   symbol:  ECG_Acquisition_IC/Design_Files/IC Design/Schematic/INV/INV.sym # of pins=4
** sym_path: Design_Files/IC Design/Schematic/INV/INV.sym
** sch_path: Design_Files/IC Design/Schematic/INV/INV.sch
.subckt INV INV_DD INV_SS INV_IN INV_OUT
*.iopin INV_DD
*.iopin INV_SS
*.ipin INV_IN
*.opin INV_OUT
XMINVP INV_OUT INV_IN INV_DD INV_DD pfet_03v3 L=0.5u W=2u nf=1 ad='int((nf+1)/2) * W/nf * 0.18u' as='int((nf+2)/2) * W/nf * 0.18u'
+ pd='2*int((nf+1)/2) * (W/nf + 0.18u)' ps='2*int((nf+2)/2) * (W/nf + 0.18u)' nrd='0.18u / W' nrs='0.18u / W'
+ sa=0 sb=0 sd=0 m=1
XMINVN INV_OUT INV_IN INV_SS INV_SS nfet_03v3 L=0.5u W=1u nf=1 ad='int((nf+1)/2) * W/nf * 0.18u' as='int((nf+2)/2) * W/nf * 0.18u'
+ pd='2*int((nf+1)/2) * (W/nf + 0.18u)' ps='2*int((nf+2)/2) * (W/nf + 0.18u)' nrd='0.18u / W' nrs='0.18u / W'
+ sa=0 sb=0 sd=0 m=1
.ends


* expanding   symbol:  ECG_Acquisition_IC/Design_Files/IC Design/Schematic/SE_OTA/SE_OTA.sym # of
*+ pins=6
** sym_path: Design_Files/IC Design/Schematic/SE_OTA/SE_OTA.sym
** sch_path: Design_Files/IC Design/Schematic/SE_OTA/SE_OTA.sch
.subckt SE_OTA SEOTA_DD SEOTA_SS SEOTA_INP SEOTA_INN SEOTA_OUT SEOTA_B
*.iopin SEOTA_DD
*.iopin SEOTA_SS
*.ipin SEOTA_INP
*.ipin SEOTA_INN
*.opin SEOTA_OUT
*.iopin SEOTA_B
XM3 net4 net4 SEOTA_DD SEOTA_DD pfet_03v3 L=4u W=1u nf=1 ad='int((nf+1)/2) * W/nf * 0.18u' as='int((nf+2)/2) * W/nf * 0.18u'
+ pd='2*int((nf+1)/2) * (W/nf + 0.18u)' ps='2*int((nf+2)/2) * (W/nf + 0.18u)' nrd='0.18u / W' nrs='0.18u / W'
+ sa=0 sb=0 sd=0 m=60
XM7 SEOTA_OUT SEOTA_B SEOTA_SS SEOTA_SS nfet_03v3 L=0.5u W=1u nf=1 ad='int((nf+1)/2) * W/nf * 0.18u'
+ as='int((nf+2)/2) * W/nf * 0.18u' pd='2*int((nf+1)/2) * (W/nf + 0.18u)' ps='2*int((nf+2)/2) * (W/nf + 0.18u)'
+ nrd='0.18u / W' nrs='0.18u / W' sa=0 sb=0 sd=0 m=100
Rz net1 net2 3.8k m=1
XM5 net3 SEOTA_B SEOTA_SS SEOTA_SS nfet_03v3 L=2u W=1u nf=1 ad='int((nf+1)/2) * W/nf * 0.18u' as='int((nf+2)/2) * W/nf * 0.18u'
+ pd='2*int((nf+1)/2) * (W/nf + 0.18u)' ps='2*int((nf+2)/2) * (W/nf + 0.18u)' nrd='0.18u / W' nrs='0.18u / W'
+ sa=0 sb=0 sd=0 m=10
XM6 SEOTA_OUT net1 SEOTA_DD SEOTA_DD pfet_03v3 L=0.5u W=1u nf=1 ad='int((nf+1)/2) * W/nf * 0.18u' as='int((nf+2)/2) * W/nf * 0.18u'
+ pd='2*int((nf+1)/2) * (W/nf + 0.18u)' ps='2*int((nf+2)/2) * (W/nf + 0.18u)' nrd='0.18u / W' nrs='0.18u / W'
+ sa=0 sb=0 sd=0 m=400
XM8 SEOTA_B SEOTA_B SEOTA_SS SEOTA_SS nfet_03v3 L=2u W=1u nf=1 ad='int((nf+1)/2) * W/nf * 0.18u' as='int((nf+2)/2) * W/nf * 0.18u'
+ pd='2*int((nf+1)/2) * (W/nf + 0.18u)' ps='2*int((nf+2)/2) * (W/nf + 0.18u)' nrd='0.18u / W' nrs='0.18u / W'
+ sa=0 sb=0 sd=0 m=20
Cc net2 SEOTA_OUT 2p m=1
XM4 net1 net4 SEOTA_DD SEOTA_DD pfet_03v3 L=4u W=1u nf=1 ad='int((nf+1)/2) * W/nf * 0.18u' as='int((nf+2)/2) * W/nf * 0.18u'
+ pd='2*int((nf+1)/2) * (W/nf + 0.18u)' ps='2*int((nf+2)/2) * (W/nf + 0.18u)' nrd='0.18u / W' nrs='0.18u / W'
+ sa=0 sb=0 sd=0 m=60
XM1 net4 SEOTA_INN net3 SEOTA_SS nfet_03v3 L=4u W=1u nf=1 ad='int((nf+1)/2) * W/nf * 0.18u' as='int((nf+2)/2) * W/nf * 0.18u'
+ pd='2*int((nf+1)/2) * (W/nf + 0.18u)' ps='2*int((nf+2)/2) * (W/nf + 0.18u)' nrd='0.18u / W' nrs='0.18u / W'
+ sa=0 sb=0 sd=0 m=400
XM2 net1 SEOTA_INP net3 SEOTA_SS nfet_03v3 L=4u W=1u nf=1 ad='int((nf+1)/2) * W/nf * 0.18u' as='int((nf+2)/2) * W/nf * 0.18u'
+ pd='2*int((nf+1)/2) * (W/nf + 0.18u)' ps='2*int((nf+2)/2) * (W/nf + 0.18u)' nrd='0.18u / W' nrs='0.18u / W'
+ sa=0 sb=0 sd=0 m=400
.ends


* expanding   symbol:  ECG_Acquisition_IC/Design_Files/IC Design/Schematic/FD_OTA/FDC/FDC.sym # of
*+ pins=8
** sym_path: Design_Files/IC Design/Schematic/FD_OTA/FDC/FDC.sym
** sch_path: Design_Files/IC Design/Schematic/FD_OTA/FDC/FDC.sch
.subckt FDC FDC_DD FDC_SS FDC_INP FDC_INN FDC_OUTN FDC_B FDC_OUTP FDC_CMFB
*.iopin FDC_DD
*.iopin FDC_SS
*.ipin FDC_INP
*.ipin FDC_INN
*.opin FDC_OUTP
*.iopin FDC_B
*.opin FDC_OUTN
*.iopin FDC_CMFB
XM3 net4 FDC_CMFB FDC_DD FDC_DD pfet_03v3 L=2u W=1u nf=1 ad='int((nf+1)/2) * W/nf * 0.18u' as='int((nf+2)/2) * W/nf * 0.18u'
+ pd='2*int((nf+1)/2) * (W/nf + 0.18u)' ps='2*int((nf+2)/2) * (W/nf + 0.18u)' nrd='0.18u / W' nrs='0.18u / W'
+ sa=0 sb=0 sd=0 m=200
XM8 FDC_OUTP FDC_B FDC_SS FDC_SS nfet_03v3 L=0.5u W=1u nf=1 ad='int((nf+1)/2) * W/nf * 0.18u' as='int((nf+2)/2) * W/nf * 0.18u'
+ pd='2*int((nf+1)/2) * (W/nf + 0.18u)' ps='2*int((nf+2)/2) * (W/nf + 0.18u)' nrd='0.18u / W' nrs='0.18u / W'
+ sa=0 sb=0 sd=0 m=100
Rz net1 net2 3.5k m=1
XM5 net3 FDC_B FDC_SS FDC_SS nfet_03v3 L=2u W=1u nf=1 ad='int((nf+1)/2) * W/nf * 0.18u' as='int((nf+2)/2) * W/nf * 0.18u'
+ pd='2*int((nf+1)/2) * (W/nf + 0.18u)' ps='2*int((nf+2)/2) * (W/nf + 0.18u)' nrd='0.18u / W' nrs='0.18u / W'
+ sa=0 sb=0 sd=0 m=10
XM6 FDC_OUTP net1 FDC_DD FDC_DD pfet_03v3 L=0.5u W=1u nf=1 ad='int((nf+1)/2) * W/nf * 0.18u' as='int((nf+2)/2) * W/nf * 0.18u'
+ pd='2*int((nf+1)/2) * (W/nf + 0.18u)' ps='2*int((nf+2)/2) * (W/nf + 0.18u)' nrd='0.18u / W' nrs='0.18u / W'
+ sa=0 sb=0 sd=0 m=200
XM10 FDC_B FDC_B FDC_SS FDC_SS nfet_03v3 L=2u W=1u nf=1 ad='int((nf+1)/2) * W/nf * 0.18u' as='int((nf+2)/2) * W/nf * 0.18u'
+ pd='2*int((nf+1)/2) * (W/nf + 0.18u)' ps='2*int((nf+2)/2) * (W/nf + 0.18u)' nrd='0.18u / W' nrs='0.18u / W'
+ sa=0 sb=0 sd=0 m=20
Cc net2 FDC_OUTP 2.5p m=1
XM9 FDC_OUTN FDC_B FDC_SS FDC_SS nfet_03v3 L=0.5u W=1u nf=1 ad='int((nf+1)/2) * W/nf * 0.18u' as='int((nf+2)/2) * W/nf * 0.18u'
+ pd='2*int((nf+1)/2) * (W/nf + 0.18u)' ps='2*int((nf+2)/2) * (W/nf + 0.18u)' nrd='0.18u / W' nrs='0.18u / W'
+ sa=0 sb=0 sd=0 m=100
Rz1 net4 net5 3.5k m=1
XM7 FDC_OUTN net4 FDC_DD FDC_DD pfet_03v3 L=0.5u W=1u nf=1 ad='int((nf+1)/2) * W/nf * 0.18u' as='int((nf+2)/2) * W/nf * 0.18u'
+ pd='2*int((nf+1)/2) * (W/nf + 0.18u)' ps='2*int((nf+2)/2) * (W/nf + 0.18u)' nrd='0.18u / W' nrs='0.18u / W'
+ sa=0 sb=0 sd=0 m=200
Cc1 net5 FDC_OUTN 2.5p m=1
XM4 net1 FDC_CMFB FDC_DD FDC_DD pfet_03v3 L=2u W=1u nf=1 ad='int((nf+1)/2) * W/nf * 0.18u' as='int((nf+2)/2) * W/nf * 0.18u'
+ pd='2*int((nf+1)/2) * (W/nf + 0.18u)' ps='2*int((nf+2)/2) * (W/nf + 0.18u)' nrd='0.18u / W' nrs='0.18u / W'
+ sa=0 sb=0 sd=0 m=200
XM1 net4 FDC_INN net3 FDC_SS nfet_03v3 L=2u W=1u nf=1 ad='int((nf+1)/2) * W/nf * 0.18u' as='int((nf+2)/2) * W/nf * 0.18u'
+ pd='2*int((nf+1)/2) * (W/nf + 0.18u)' ps='2*int((nf+2)/2) * (W/nf + 0.18u)' nrd='0.18u / W' nrs='0.18u / W'
+ sa=0 sb=0 sd=0 m=200
XM2 net1 FDC_INP net3 FDC_SS nfet_03v3 L=2u W=1u nf=1 ad='int((nf+1)/2) * W/nf * 0.18u' as='int((nf+2)/2) * W/nf * 0.18u'
+ pd='2*int((nf+1)/2) * (W/nf + 0.18u)' ps='2*int((nf+2)/2) * (W/nf + 0.18u)' nrd='0.18u / W' nrs='0.18u / W'
+ sa=0 sb=0 sd=0 m=200
.ends


* expanding   symbol:  ECG_Acquisition_IC/Design_Files/IC Design/Schematic/FD_OTA/CMFB/CMFB.sym # of
*+ pins=6
** sym_path: Design_Files/IC Design/Schematic/FD_OTA/CMFB/CMFB.sym
** sch_path: Design_Files/IC Design/Schematic/FD_OTA/CMFB/CMFB.sch
.subckt CMFB CMFB_DD CMFB_SS CMFB_IN CMFB_REF CMFB_OUT CMFB_B
*.iopin CMFB_DD
*.iopin CMFB_SS
*.ipin CMFB_IN
*.ipin CMFB_REF
*.opin CMFB_OUT
*.iopin CMFB_B
XM4 CMFB_OUT CMFB_OUT CMFB_DD CMFB_DD pfet_03v3 L=0.5u W=1u nf=1 ad='int((nf+1)/2) * W/nf * 0.18u' as='int((nf+2)/2) * W/nf * 0.18u'
+ pd='2*int((nf+1)/2) * (W/nf + 0.18u)' ps='2*int((nf+2)/2) * (W/nf + 0.18u)' nrd='0.18u / W' nrs='0.18u / W'
+ sa=0 sb=0 sd=0 m=77
XM3 net2 net2 CMFB_DD CMFB_DD pfet_03v3 L=0.5u W=1u nf=1 ad='int((nf+1)/2) * W/nf * 0.18u' as='int((nf+2)/2) * W/nf * 0.18u'
+ pd='2*int((nf+1)/2) * (W/nf + 0.18u)' ps='2*int((nf+2)/2) * (W/nf + 0.18u)' nrd='0.18u / W' nrs='0.18u / W'
+ sa=0 sb=0 sd=0 m=77
XM1 net2 CMFB_REF net1 CMFB_SS nfet_03v3 L=0.5u W=1u nf=1 ad='int((nf+1)/2) * W/nf * 0.18u' as='int((nf+2)/2) * W/nf * 0.18u'
+ pd='2*int((nf+1)/2) * (W/nf + 0.18u)' ps='2*int((nf+2)/2) * (W/nf + 0.18u)' nrd='0.18u / W' nrs='0.18u / W'
+ sa=0 sb=0 sd=0 m=5
XM2 CMFB_OUT CMFB_IN net1 CMFB_SS nfet_03v3 L=0.5u W=1u nf=1 ad='int((nf+1)/2) * W/nf * 0.18u' as='int((nf+2)/2) * W/nf * 0.18u'
+ pd='2*int((nf+1)/2) * (W/nf + 0.18u)' ps='2*int((nf+2)/2) * (W/nf + 0.18u)' nrd='0.18u / W' nrs='0.18u / W'
+ sa=0 sb=0 sd=0 m=5
XM5 net1 CMFB_B CMFB_SS CMFB_SS nfet_03v3 L=2u W=1u nf=1 ad='int((nf+1)/2) * W/nf * 0.18u' as='int((nf+2)/2) * W/nf * 0.18u'
+ pd='2*int((nf+1)/2) * (W/nf + 0.18u)' ps='2*int((nf+2)/2) * (W/nf + 0.18u)' nrd='0.18u / W' nrs='0.18u / W'
+ sa=0 sb=0 sd=0 m=20
XM10 CMFB_B CMFB_B CMFB_SS CMFB_SS nfet_03v3 L=2u W=1u nf=1 ad='int((nf+1)/2) * W/nf * 0.18u' as='int((nf+2)/2) * W/nf * 0.18u'
+ pd='2*int((nf+1)/2) * (W/nf + 0.18u)' ps='2*int((nf+2)/2) * (W/nf + 0.18u)' nrd='0.18u / W' nrs='0.18u / W'
+ sa=0 sb=0 sd=0 m=20
.ends

.end
